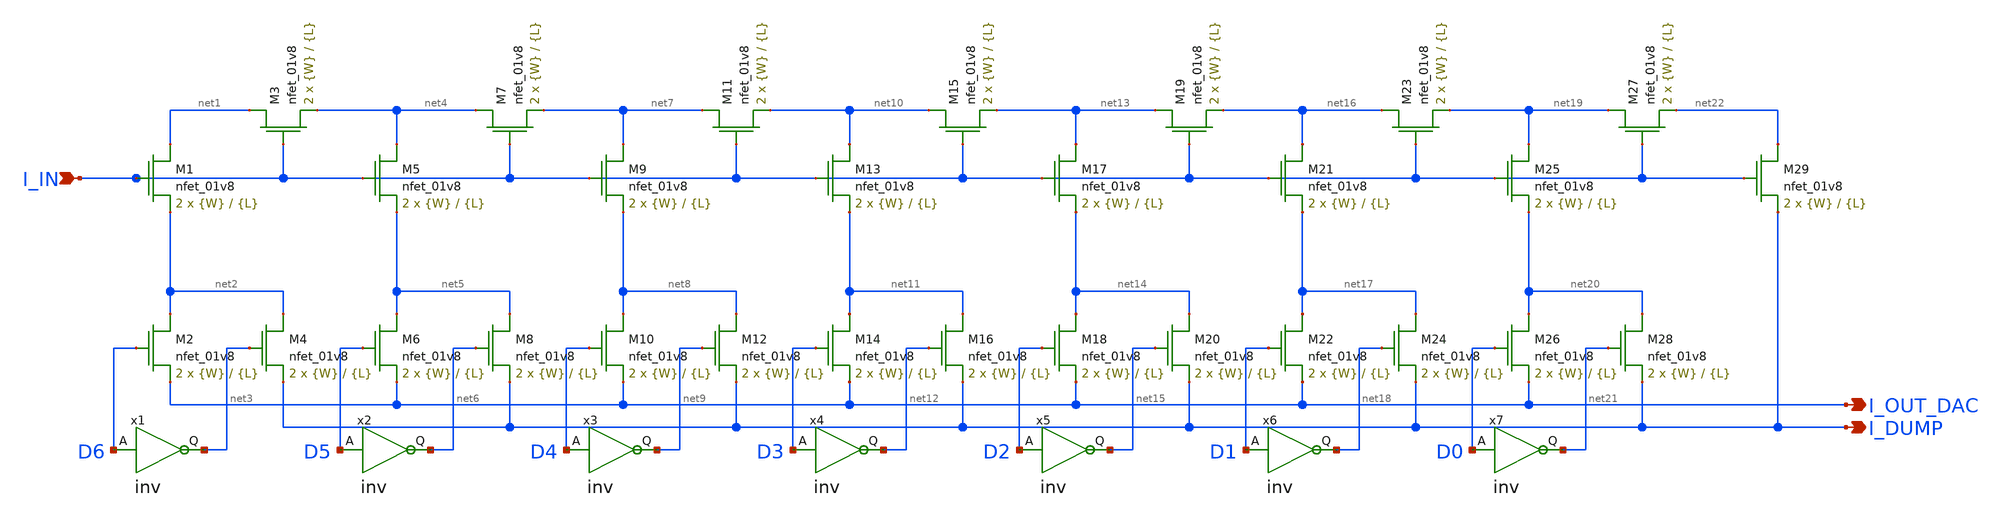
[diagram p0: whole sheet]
** sch_path: schemas/M2M_ladder.sch
**.subckt M2M_ladder I_OUT_DAC I_DUMP I_IN
*.opin I_OUT_DAC
*.opin I_DUMP
*.ipin I_IN
XM1 net1 I_IN net2 GND sky130_fd_pr__nfet_01v8 L={L} W={W} nf=1 ad='int((nf+1)/2) * W/nf * 0.29' as='int((nf+2)/2) * W/nf * 0.29'
+ pd='2*int((nf+1)/2) * (W/nf + 0.29)' ps='2*int((nf+2)/2) * (W/nf + 0.29)' nrd='0.29 / W' nrs='0.29 / W'
+ sa=0 sb=0 sd=0 mult=2 m=2
XM2 net2 D6 I_OUT_DAC GND sky130_fd_pr__nfet_01v8 L={L} W={W} nf=1 ad='int((nf+1)/2) * W/nf * 0.29' as='int((nf+2)/2) * W/nf * 0.29'
+ pd='2*int((nf+1)/2) * (W/nf + 0.29)' ps='2*int((nf+2)/2) * (W/nf + 0.29)' nrd='0.29 / W' nrs='0.29 / W'
+ sa=0 sb=0 sd=0 mult=2 m=2
XM3 net1 I_IN net4 GND sky130_fd_pr__nfet_01v8 L={L} W={W} nf=1 ad='int((nf+1)/2) * W/nf * 0.29' as='int((nf+2)/2) * W/nf * 0.29'
+ pd='2*int((nf+1)/2) * (W/nf + 0.29)' ps='2*int((nf+2)/2) * (W/nf + 0.29)' nrd='0.29 / W' nrs='0.29 / W'
+ sa=0 sb=0 sd=0 mult=2 m=2
XM4 net2 net3 I_DUMP GND sky130_fd_pr__nfet_01v8 L={L} W={W} nf=1 ad='int((nf+1)/2) * W/nf * 0.29' as='int((nf+2)/2) * W/nf * 0.29'
+ pd='2*int((nf+1)/2) * (W/nf + 0.29)' ps='2*int((nf+2)/2) * (W/nf + 0.29)' nrd='0.29 / W' nrs='0.29 / W'
+ sa=0 sb=0 sd=0 mult=2 m=2
XM5 net4 I_IN net5 GND sky130_fd_pr__nfet_01v8 L={L} W={W} nf=1 ad='int((nf+1)/2) * W/nf * 0.29' as='int((nf+2)/2) * W/nf * 0.29'
+ pd='2*int((nf+1)/2) * (W/nf + 0.29)' ps='2*int((nf+2)/2) * (W/nf + 0.29)' nrd='0.29 / W' nrs='0.29 / W'
+ sa=0 sb=0 sd=0 mult=2 m=2
XM6 net5 D5 I_OUT_DAC GND sky130_fd_pr__nfet_01v8 L={L} W={W} nf=1 ad='int((nf+1)/2) * W/nf * 0.29' as='int((nf+2)/2) * W/nf * 0.29'
+ pd='2*int((nf+1)/2) * (W/nf + 0.29)' ps='2*int((nf+2)/2) * (W/nf + 0.29)' nrd='0.29 / W' nrs='0.29 / W'
+ sa=0 sb=0 sd=0 mult=2 m=2
XM7 net4 I_IN net7 GND sky130_fd_pr__nfet_01v8 L={L} W={W} nf=1 ad='int((nf+1)/2) * W/nf * 0.29' as='int((nf+2)/2) * W/nf * 0.29'
+ pd='2*int((nf+1)/2) * (W/nf + 0.29)' ps='2*int((nf+2)/2) * (W/nf + 0.29)' nrd='0.29 / W' nrs='0.29 / W'
+ sa=0 sb=0 sd=0 mult=2 m=2
XM8 net5 net6 I_DUMP GND sky130_fd_pr__nfet_01v8 L={L} W={W} nf=1 ad='int((nf+1)/2) * W/nf * 0.29' as='int((nf+2)/2) * W/nf * 0.29'
+ pd='2*int((nf+1)/2) * (W/nf + 0.29)' ps='2*int((nf+2)/2) * (W/nf + 0.29)' nrd='0.29 / W' nrs='0.29 / W'
+ sa=0 sb=0 sd=0 mult=2 m=2
XM9 net7 I_IN net8 GND sky130_fd_pr__nfet_01v8 L={L} W={W} nf=1 ad='int((nf+1)/2) * W/nf * 0.29' as='int((nf+2)/2) * W/nf * 0.29'
+ pd='2*int((nf+1)/2) * (W/nf + 0.29)' ps='2*int((nf+2)/2) * (W/nf + 0.29)' nrd='0.29 / W' nrs='0.29 / W'
+ sa=0 sb=0 sd=0 mult=2 m=2
XM10 net8 D4 I_OUT_DAC GND sky130_fd_pr__nfet_01v8 L={L} W={W} nf=1 ad='int((nf+1)/2) * W/nf * 0.29'
+ as='int((nf+2)/2) * W/nf * 0.29' pd='2*int((nf+1)/2) * (W/nf + 0.29)' ps='2*int((nf+2)/2) * (W/nf + 0.29)'
+ nrd='0.29 / W' nrs='0.29 / W' sa=0 sb=0 sd=0 mult=2 m=2
XM11 net7 I_IN net10 GND sky130_fd_pr__nfet_01v8 L={L} W={W} nf=1 ad='int((nf+1)/2) * W/nf * 0.29' as='int((nf+2)/2) * W/nf * 0.29'
+ pd='2*int((nf+1)/2) * (W/nf + 0.29)' ps='2*int((nf+2)/2) * (W/nf + 0.29)' nrd='0.29 / W' nrs='0.29 / W'
+ sa=0 sb=0 sd=0 mult=2 m=2
XM12 net8 net9 I_DUMP GND sky130_fd_pr__nfet_01v8 L={L} W={W} nf=1 ad='int((nf+1)/2) * W/nf * 0.29' as='int((nf+2)/2) * W/nf * 0.29'
+ pd='2*int((nf+1)/2) * (W/nf + 0.29)' ps='2*int((nf+2)/2) * (W/nf + 0.29)' nrd='0.29 / W' nrs='0.29 / W'
+ sa=0 sb=0 sd=0 mult=2 m=2
XM13 net10 I_IN net11 GND sky130_fd_pr__nfet_01v8 L={L} W={W} nf=1 ad='int((nf+1)/2) * W/nf * 0.29' as='int((nf+2)/2) * W/nf * 0.29'
+ pd='2*int((nf+1)/2) * (W/nf + 0.29)' ps='2*int((nf+2)/2) * (W/nf + 0.29)' nrd='0.29 / W' nrs='0.29 / W'
+ sa=0 sb=0 sd=0 mult=2 m=2
XM14 net11 D3 I_OUT_DAC GND sky130_fd_pr__nfet_01v8 L={L} W={W} nf=1 ad='int((nf+1)/2) * W/nf * 0.29'
+ as='int((nf+2)/2) * W/nf * 0.29' pd='2*int((nf+1)/2) * (W/nf + 0.29)' ps='2*int((nf+2)/2) * (W/nf + 0.29)'
+ nrd='0.29 / W' nrs='0.29 / W' sa=0 sb=0 sd=0 mult=2 m=2
XM15 net10 I_IN net13 GND sky130_fd_pr__nfet_01v8 L={L} W={W} nf=1 ad='int((nf+1)/2) * W/nf * 0.29' as='int((nf+2)/2) * W/nf * 0.29'
+ pd='2*int((nf+1)/2) * (W/nf + 0.29)' ps='2*int((nf+2)/2) * (W/nf + 0.29)' nrd='0.29 / W' nrs='0.29 / W'
+ sa=0 sb=0 sd=0 mult=2 m=2
XM16 net11 net12 I_DUMP GND sky130_fd_pr__nfet_01v8 L={L} W={W} nf=1 ad='int((nf+1)/2) * W/nf * 0.29'
+ as='int((nf+2)/2) * W/nf * 0.29' pd='2*int((nf+1)/2) * (W/nf + 0.29)' ps='2*int((nf+2)/2) * (W/nf + 0.29)'
+ nrd='0.29 / W' nrs='0.29 / W' sa=0 sb=0 sd=0 mult=2 m=2
XM17 net13 I_IN net14 GND sky130_fd_pr__nfet_01v8 L={L} W={W} nf=1 ad='int((nf+1)/2) * W/nf * 0.29' as='int((nf+2)/2) * W/nf * 0.29'
+ pd='2*int((nf+1)/2) * (W/nf + 0.29)' ps='2*int((nf+2)/2) * (W/nf + 0.29)' nrd='0.29 / W' nrs='0.29 / W'
+ sa=0 sb=0 sd=0 mult=2 m=2
XM18 net14 D2 I_OUT_DAC GND sky130_fd_pr__nfet_01v8 L={L} W={W} nf=1 ad='int((nf+1)/2) * W/nf * 0.29'
+ as='int((nf+2)/2) * W/nf * 0.29' pd='2*int((nf+1)/2) * (W/nf + 0.29)' ps='2*int((nf+2)/2) * (W/nf + 0.29)'
+ nrd='0.29 / W' nrs='0.29 / W' sa=0 sb=0 sd=0 mult=2 m=2
XM19 net13 I_IN net16 GND sky130_fd_pr__nfet_01v8 L={L} W={W} nf=1 ad='int((nf+1)/2) * W/nf * 0.29' as='int((nf+2)/2) * W/nf * 0.29'
+ pd='2*int((nf+1)/2) * (W/nf + 0.29)' ps='2*int((nf+2)/2) * (W/nf + 0.29)' nrd='0.29 / W' nrs='0.29 / W'
+ sa=0 sb=0 sd=0 mult=2 m=2
XM20 net14 net15 I_DUMP GND sky130_fd_pr__nfet_01v8 L={L} W={W} nf=1 ad='int((nf+1)/2) * W/nf * 0.29'
+ as='int((nf+2)/2) * W/nf * 0.29' pd='2*int((nf+1)/2) * (W/nf + 0.29)' ps='2*int((nf+2)/2) * (W/nf + 0.29)'
+ nrd='0.29 / W' nrs='0.29 / W' sa=0 sb=0 sd=0 mult=2 m=2
XM21 net16 I_IN net17 GND sky130_fd_pr__nfet_01v8 L={L} W={W} nf=1 ad='int((nf+1)/2) * W/nf * 0.29' as='int((nf+2)/2) * W/nf * 0.29'
+ pd='2*int((nf+1)/2) * (W/nf + 0.29)' ps='2*int((nf+2)/2) * (W/nf + 0.29)' nrd='0.29 / W' nrs='0.29 / W'
+ sa=0 sb=0 sd=0 mult=2 m=2
XM22 net17 D1 I_OUT_DAC GND sky130_fd_pr__nfet_01v8 L={L} W={W} nf=1 ad='int((nf+1)/2) * W/nf * 0.29'
+ as='int((nf+2)/2) * W/nf * 0.29' pd='2*int((nf+1)/2) * (W/nf + 0.29)' ps='2*int((nf+2)/2) * (W/nf + 0.29)'
+ nrd='0.29 / W' nrs='0.29 / W' sa=0 sb=0 sd=0 mult=2 m=2
XM23 net16 I_IN net19 GND sky130_fd_pr__nfet_01v8 L={L} W={W} nf=1 ad='int((nf+1)/2) * W/nf * 0.29' as='int((nf+2)/2) * W/nf * 0.29'
+ pd='2*int((nf+1)/2) * (W/nf + 0.29)' ps='2*int((nf+2)/2) * (W/nf + 0.29)' nrd='0.29 / W' nrs='0.29 / W'
+ sa=0 sb=0 sd=0 mult=2 m=2
XM24 net17 net18 I_DUMP GND sky130_fd_pr__nfet_01v8 L={L} W={W} nf=1 ad='int((nf+1)/2) * W/nf * 0.29'
+ as='int((nf+2)/2) * W/nf * 0.29' pd='2*int((nf+1)/2) * (W/nf + 0.29)' ps='2*int((nf+2)/2) * (W/nf + 0.29)'
+ nrd='0.29 / W' nrs='0.29 / W' sa=0 sb=0 sd=0 mult=2 m=2
XM25 net19 I_IN net20 GND sky130_fd_pr__nfet_01v8 L={L} W={W} nf=1 ad='int((nf+1)/2) * W/nf * 0.29' as='int((nf+2)/2) * W/nf * 0.29'
+ pd='2*int((nf+1)/2) * (W/nf + 0.29)' ps='2*int((nf+2)/2) * (W/nf + 0.29)' nrd='0.29 / W' nrs='0.29 / W'
+ sa=0 sb=0 sd=0 mult=2 m=2
XM26 net20 D0 I_OUT_DAC GND sky130_fd_pr__nfet_01v8 L={L} W={W} nf=1 ad='int((nf+1)/2) * W/nf * 0.29'
+ as='int((nf+2)/2) * W/nf * 0.29' pd='2*int((nf+1)/2) * (W/nf + 0.29)' ps='2*int((nf+2)/2) * (W/nf + 0.29)'
+ nrd='0.29 / W' nrs='0.29 / W' sa=0 sb=0 sd=0 mult=2 m=2
XM27 net19 I_IN net22 GND sky130_fd_pr__nfet_01v8 L={L} W={W} nf=1 ad='int((nf+1)/2) * W/nf * 0.29' as='int((nf+2)/2) * W/nf * 0.29'
+ pd='2*int((nf+1)/2) * (W/nf + 0.29)' ps='2*int((nf+2)/2) * (W/nf + 0.29)' nrd='0.29 / W' nrs='0.29 / W'
+ sa=0 sb=0 sd=0 mult=2 m=2
XM28 net20 net21 I_DUMP GND sky130_fd_pr__nfet_01v8 L={L} W={W} nf=1 ad='int((nf+1)/2) * W/nf * 0.29'
+ as='int((nf+2)/2) * W/nf * 0.29' pd='2*int((nf+1)/2) * (W/nf + 0.29)' ps='2*int((nf+2)/2) * (W/nf + 0.29)'
+ nrd='0.29 / W' nrs='0.29 / W' sa=0 sb=0 sd=0 mult=2 m=2
XM29 net22 I_IN I_DUMP GND sky130_fd_pr__nfet_01v8 L={L} W={W} nf=1 ad='int((nf+1)/2) * W/nf * 0.29'
+ as='int((nf+2)/2) * W/nf * 0.29' pd='2*int((nf+1)/2) * (W/nf + 0.29)' ps='2*int((nf+2)/2) * (W/nf + 0.29)'
+ nrd='0.29 / W' nrs='0.29 / W' sa=0 sb=0 sd=0 mult=2 m=2
x1 net3 D6 inv
x2 net6 D5 inv
x3 net9 D4 inv
x4 net12 D3 inv
x5 net15 D2 inv
x6 net18 D1 inv
x7 net21 D0 inv
**.ends

* expanding   symbol:  /home/mstopyra/Documents/MADVLSI-MP4-DAC/schemas/inv.sym # of pins=2
** sym_path: /home/mstopyra/Documents/MADVLSI-MP4-DAC/schemas/inv.sym
** sch_path: /home/mstopyra/Documents/MADVLSI-MP4-DAC/schemas/inv.sch
.subckt inv Q A
*.ipin A
*.opin Q
XM1 Q A GND GND sky130_fd_pr__nfet_01v8 L=4 W=32 nf=1 ad='int((nf+1)/2) * W/nf * 0.29' as='int((nf+2)/2) * W/nf * 0.29'
+ pd='2*int((nf+1)/2) * (W/nf + 0.29)' ps='2*int((nf+2)/2) * (W/nf + 0.29)' nrd='0.29 / W' nrs='0.29 / W'
+ sa=0 sb=0 sd=0 mult=2 m=2
XM2 Q A VDD VDD sky130_fd_pr__pfet_01v8 L=4 W=32 nf=1 ad='int((nf+1)/2) * W/nf * 0.29' as='int((nf+2)/2) * W/nf * 0.29'
+ pd='2*int((nf+1)/2) * (W/nf + 0.29)' ps='2*int((nf+2)/2) * (W/nf + 0.29)' nrd='0.29 / W' nrs='0.29 / W'
+ sa=0 sb=0 sd=0 mult=1 m=1
.ends

.GLOBAL VDD
.GLOBAL GND
.end
